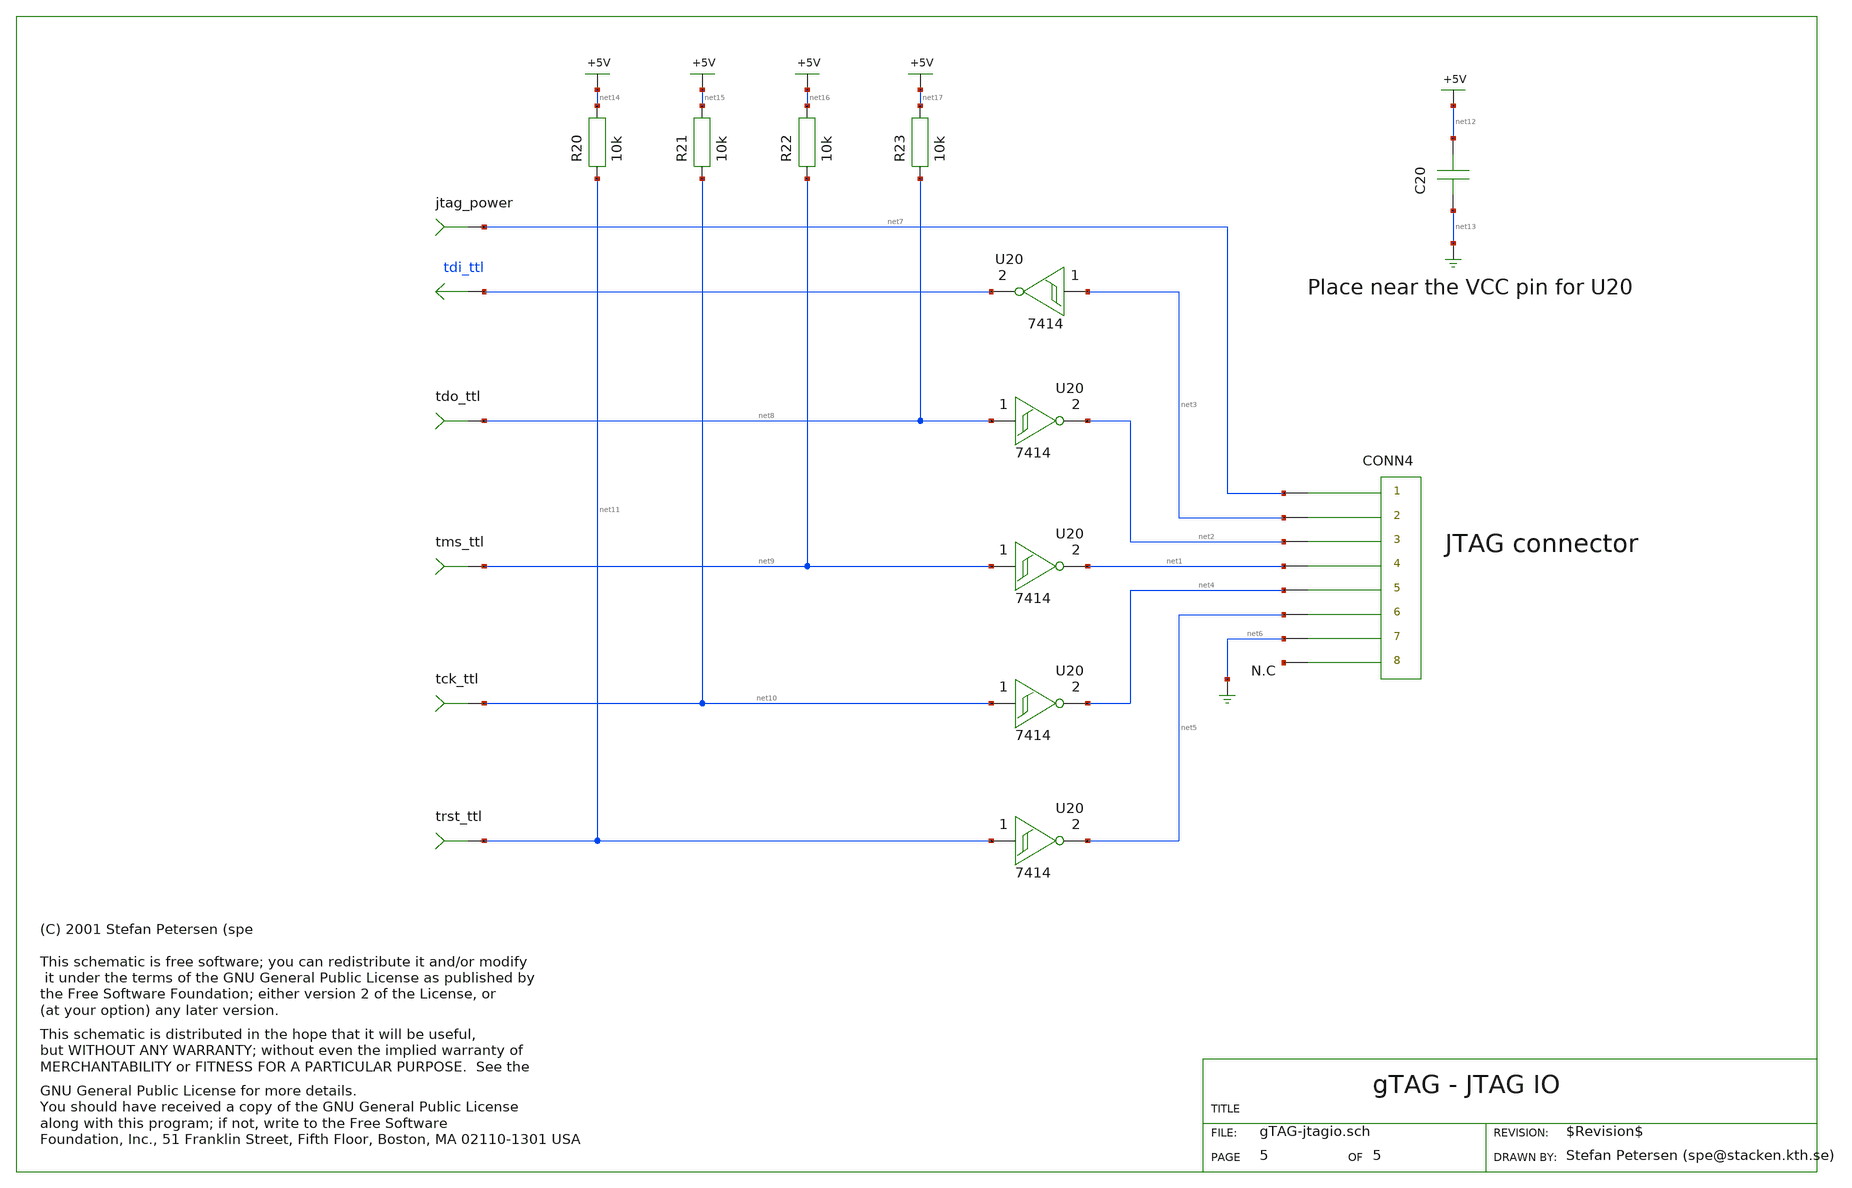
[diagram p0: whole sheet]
** sch_path: xschem_library/gschem_import/gTAG-jtagio.sch
* copyleft.sym
**.subckt gTAG-jtagio tdi_ttl
tdo_ttl net8
tms_ttl net9
tck_ttl net10
trst_ttl net11
jtag_power net7
U20 net3 tdi_ttl
U20 net8 net2
U20 net9 net1
U20 net10 net4
U20 net11 net5
CONN4 net7 net3 net2 net1 net4 net5 net6 net18
C20 net13 net12 100n
R20 net11 net14 10k
R21 net10 net15 10k
R22 net9 net16 10k
R23 net8 net17 10k
**.ends
.end
